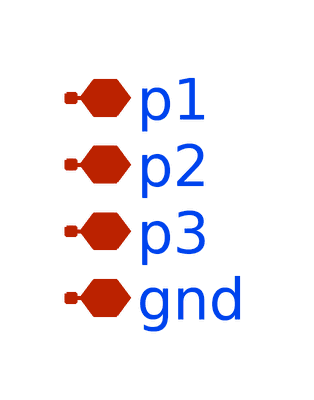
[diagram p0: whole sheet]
** sch_path: xschem/vco/parts/coil.sch
**.subckt coil p1 p2 p3 gnd
*.iopin p1
*.iopin p2
*.iopin p3
*.iopin gnd
**** begin user architecture code


.subckt ind p1 p2 p3 gnd
l1_sect1 p1 _n1i_sect1 6.622980e-10
l2_sect1 _n2i_sect1 p2 6.622980e-10
r1_sect1 _n1i_sect1 _n_sect1 1.976849e+00
r2_sect1 _n_sect1 _n2i_sect1 1.976849e+00
lc_sect1 _nc_sect1 p3 1.581139e-11
rc_sect1 _n_sect1 _nc_sect1 3.537294e-02
l1_sect2 p1 _n1i_sect2 2.784725e-09
l2_sect2 _n2i_sect2 p2 2.784725e-09
r1_sect2 _n1i_sect2 _n_sect2 1.905337e+02
r2_sect2 _n_sect2 _n2i_sect2 1.905337e+02
lc_sect2 _nc_sect2 p3 1.581139e-11
rc_sect2 _n_sect2 _nc_sect2 1.581139e-02
k12_sect1 l1_sect1 l2_sect1 6.284125e-01
k12_sect2 l1_sect2 l2_sect2 6.284125e-01
ks1s2_1 l1_sect1 l1_sect2 3.715239e-01
ks1s2_2 l2_sect1 l2_sect2 3.715239e-01
c12 p1 p2 1.746590e-14
c13 p1 p3 1.581139e-17
c23 p2 p3 1.581139e-17
c_1_sub p1 _n1_1_sub 4.699668e-14
rs_1_sub _n1_1_sub gnd 1.676673e+01
cs_1_sub _n1_1_sub gnd 1.581139e-17
c_2_sub p2 _n1_2_sub 4.699668e-14
rs_2_sub _n1_2_sub gnd 1.676673e+01
cs_2_sub _n1_2_sub gnd 1.581139e-17
c_3_sub p3 _n1_3_sub 2.790193e-14
rs_3_sub _n1_3_sub gnd 9.455176e+02
cs_3_sub _n1_3_sub gnd 1.581139e-17
.ends

**** end user architecture code
**.ends
.end
